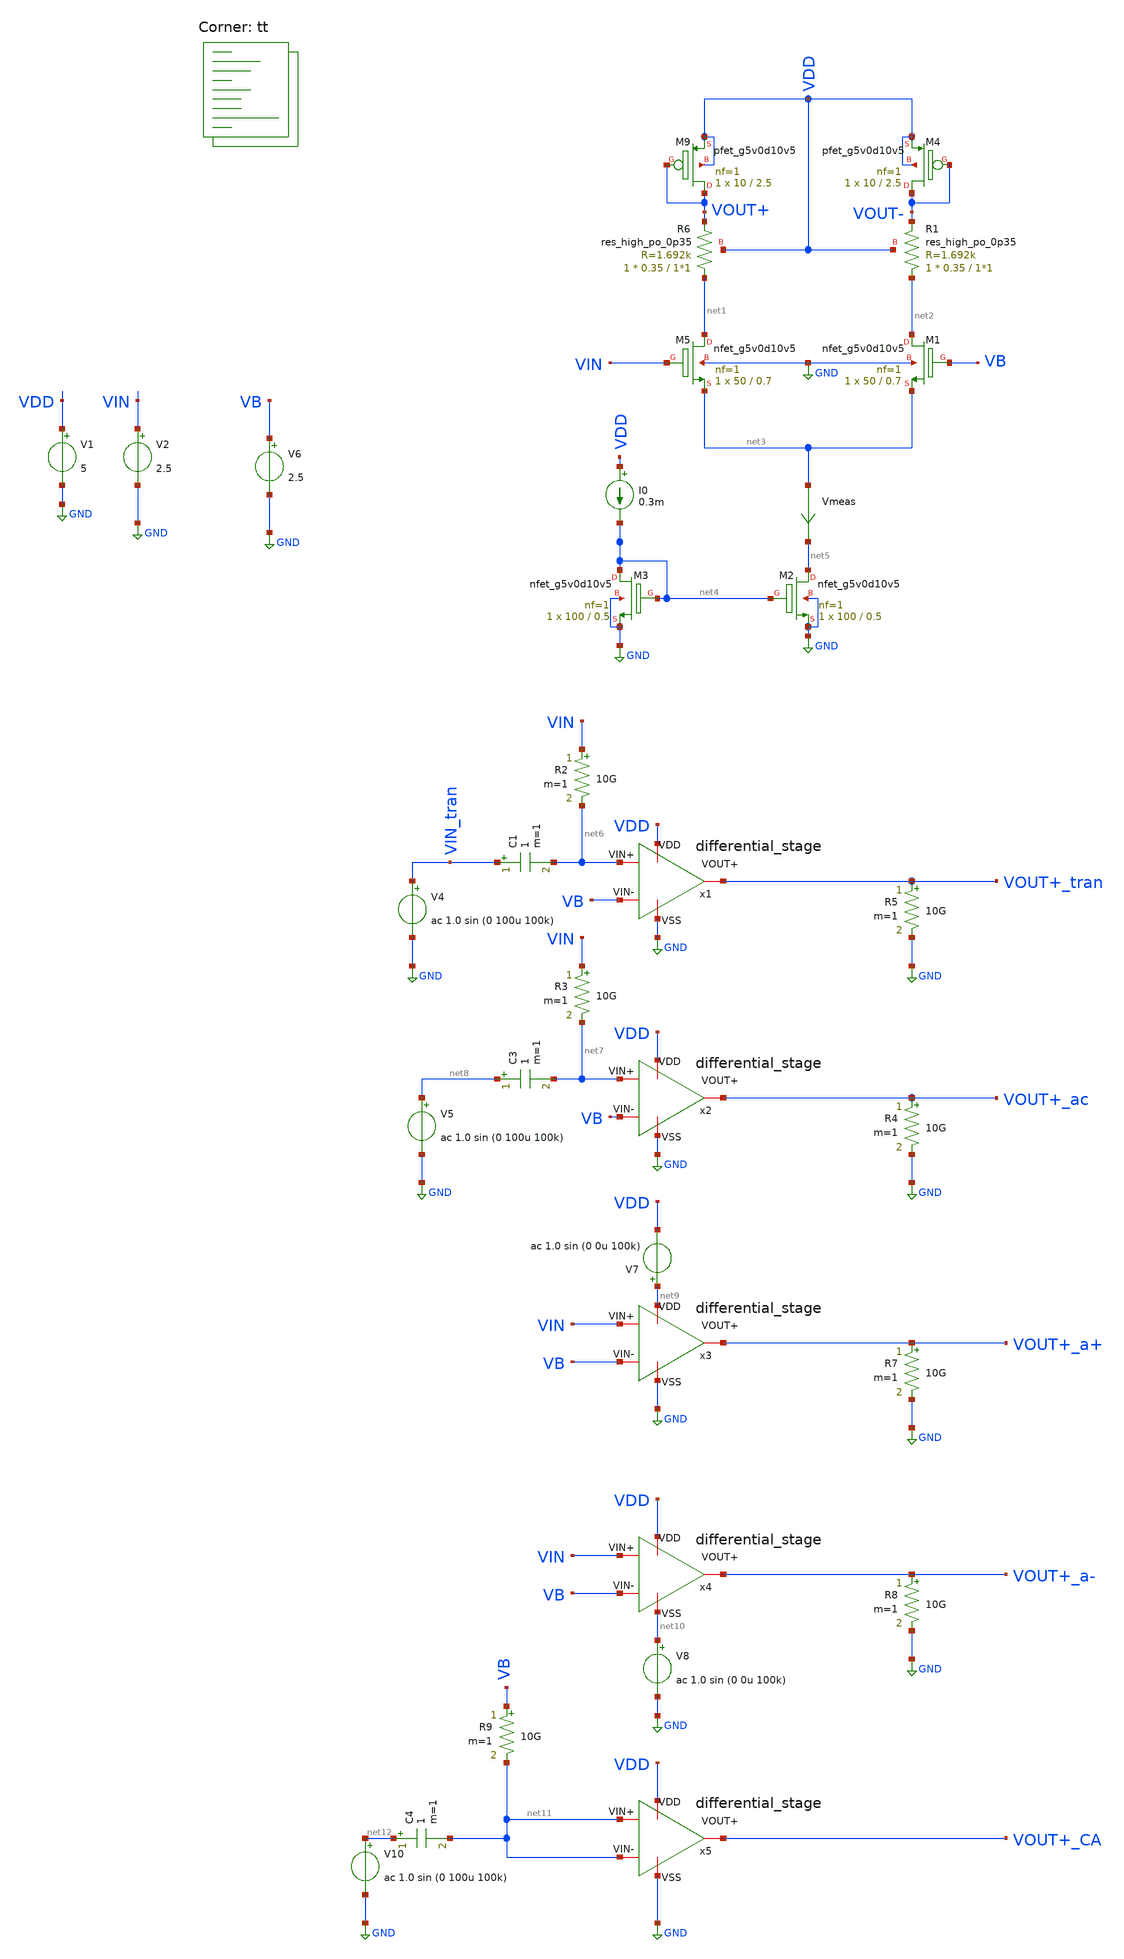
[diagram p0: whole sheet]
** sch_path: amplifiers/differencial_stage_amps/stange stages/with more impedance/diferential_stage.sch
**.subckt diferential_stage
XM5 net1 VIN net3 GND sky130_fd_pr__nfet_g5v0d10v5 L=0.7 W=50 nf=1 ad='int((1 + 1)/2) * 50 / 1 * 0.29'
+ as='int((1 + 2)/2) * 50 / 1 * 0.29' pd='2*int((1 + 1)/2) * (50 / 1 + 0.29)' ps='2*int((1 + 2)/2) * (50 / 1 + 0.29)'
+ nrd='0.29 / 50 ' nrs='0.29 / 50 ' sa=0 sb=0 sd=0 mult=1 m=1
XM1 net2 VB net3 GND sky130_fd_pr__nfet_g5v0d10v5 L=0.7 W=50 nf=1 ad='int((1 + 1)/2) * 50 / 1 * 0.29'
+ as='int((1 + 2)/2) * 50 / 1 * 0.29' pd='2*int((1 + 1)/2) * (50 / 1 + 0.29)' ps='2*int((1 + 2)/2) * (50 / 1 + 0.29)'
+ nrd='0.29 / 50 ' nrs='0.29 / 50 ' sa=0 sb=0 sd=0 mult=1 m=1
V1 VDD GND 5
V2 VIN GND 2.5
V6 VB GND 2.5
XM2 net5 net4 GND GND sky130_fd_pr__nfet_g5v0d10v5 L=0.5 W=100 nf=1 ad='int((1 + 1)/2) * 100 / 1 * 0.29'
+ as='int((1 + 2)/2) * 100 / 1 * 0.29' pd='2*int((1 + 1)/2) * (100 / 1 + 0.29)' ps='2*int((1 + 2)/2) * (100 / 1 + 0.29)'
+ nrd='0.29 / 100 ' nrs='0.29 / 100 ' sa=0 sb=0 sd=0 mult=1 m=1
Vmeas net3 net5 0
.save i(vmeas)
R5 VOUT+_tran GND 10G m=1
R2 VIN net6 10G m=1
V4 VIN_tran GND ac 1.0 sin (0 100u 100k)
C1 VIN_tran net6 1 m=1
R3 VIN net7 10G m=1
C3 net8 net7 1 m=1
V5 net8 GND ac 1.0 sin (0 100u 100k)
R4 VOUT+_ac GND 10G m=1
V7 net9 VDD ac 1.0 sin (0 0u 100k)
R7 VOUT+_a+ GND 10G m=1
V8 net10 GND ac 1.0 sin (0 0u 100k)
R8 VOUT+_a- GND 10G m=1
R9 VB net11 10G m=1
C4 net12 net11 1 m=1
V10 net12 GND ac 1.0 sin (0 100u 100k)
XM3 net4 net4 GND GND sky130_fd_pr__nfet_g5v0d10v5 L=0.5 W=100 nf=1 ad='int((1 + 1)/2) * 100 / 1 * 0.29'
+ as='int((1 + 2)/2) * 100 / 1 * 0.29' pd='2*int((1 + 1)/2) * (100 / 1 + 0.29)' ps='2*int((1 + 2)/2) * (100 / 1 + 0.29)'
+ nrd='0.29 / 100 ' nrs='0.29 / 100 ' sa=0 sb=0 sd=0 mult=1 m=1
I0 VDD net4 0.3m
XM9 VOUT+ VOUT+ VDD VDD sky130_fd_pr__pfet_g5v0d10v5 L=2.5 W=10 nf=1 ad='int((1 + 1)/2) * 10 / 1 * 0.29'
+ as='int((1 + 2)/2) * 10 / 1 * 0.29' pd='2*int((1 + 1)/2) * (10 / 1 + 0.29)' ps='2*int((1 + 2)/2) * (10 / 1 + 0.29)'
+ nrd='0.29 / 10 ' nrs='0.29 / 10 ' sa=0 sb=0 sd=0 mult=1 m=1
XM4 VOUT- VOUT- VDD VDD sky130_fd_pr__pfet_g5v0d10v5 L=2.5 W=10 nf=1 ad='int((1 + 1)/2) * 10 / 1 * 0.29'
+ as='int((1 + 2)/2) * 10 / 1 * 0.29' pd='2*int((1 + 1)/2) * (10 / 1 + 0.29)' ps='2*int((1 + 2)/2) * (10 / 1 + 0.29)'
+ nrd='0.29 / 10 ' nrs='0.29 / 10 ' sa=0 sb=0 sd=0 mult=1 m=1
XR6 net1 VOUT+ VDD sky130_fd_pr__res_high_po_0p35 L=1*1 mult=1 m=1
XR1 net2 VOUT- VDD sky130_fd_pr__res_high_po_0p35 L=1*1 mult=1 m=1
x1 VDD GND net6 VB VOUT+_tran differential_stage
x2 VDD GND net7 VB VOUT+_ac differential_stage
x3 net9 GND VIN VB VOUT+_a+ differential_stage
x4 VDD net10 VIN VB VOUT+_a- differential_stage
x5 VDD GND net11 net11 VOUT+_CA differential_stage
**** begin user architecture code

**************************************************************
**************************************************************
**************************************************************
**************************************************************
**************************************************************
*LIBs*********************************************************
**************************************************************
**************************************************************
**************************************************************
**************************************************************
**************************************************************
*.lib $::SKYWATER_MODELS/sky130.lib.spice tt
* chose the corners in the corner file
* tt_mm for mismatch
* ss ff sf fs standart corners
* ll hh lh hl capacitor and resistors corners
* mc for total process variation including corners
**************************************************************
**************************************************************
**************************************************************
**************************************************************
**************************************************************
*Corners/montecarlo options***********************************
**************************************************************
**************************************************************
**************************************************************
**************************************************************
**************************************************************
.TEMP 27
**************************************************************
**************************************************************
**************************************************************
**************************************************************
*SIMULATION and Plots*****************************************
**************************************************************
**************************************************************
**************************************************************
**************************************************************
.control
save all
dc V2 0 5 0.01
*dc simulation
plot v(VOUT-) v(VIN) deriv(v(VOUT-)) v(VOUT+) deriv(v(VOUT+))
*ploting VIN VOUT and the voltage gain
plot i(Vmeas)
*ploting the current for curiosity
tran 1ns 20u
*transient simulation
plot (v(VOUT+_tran))
*simple plot to exemplify the gain
fft v(VOUT+_tran) v(VIN_tran)
*fast fourier transfor
plot mag(v(VOUT+_tran)) mag(v(VIN_tran))
ac dec 20 1 1000G
*simple ac simulation
plot db(v(VOUT+_ac))
plot db(v(VOUT+_a+))
plot db(v(VOUT+_a-))
plot db(v(VOUT+_CA))
plot db((v(VOUT+_ac))/(v(VOUT+_CA)))
plot db((v(VOUT+_ac))/(v(VOUT+_a+)))
plot db((v(VOUT+_ac))/(v(VOUT+_a-)))
.endc

.lib $::SKYWATER_MODELS/sky130.lib.spice tt
**** end user architecture code
**.ends
.GLOBAL GND
.end
